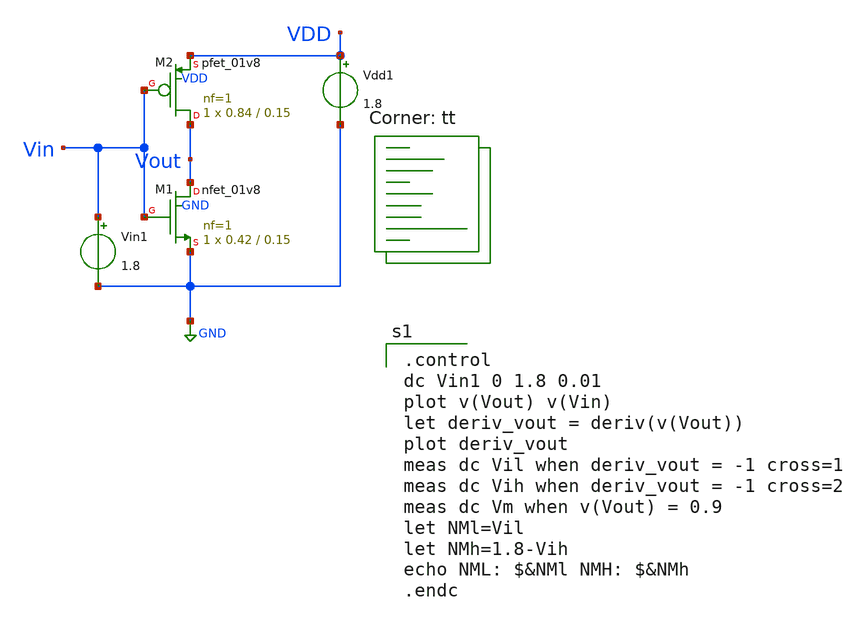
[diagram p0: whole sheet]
** sch_path: tut2/expt2_0/expt2_0.sch
**.subckt expt2_0
XM1 Vout Vin GND GND sky130_fd_pr__nfet_01v8 L=0.15 W=0.42 nf=1 ad='int((nf+1)/2) * W/nf * 0.29' as='int((nf+2)/2) * W/nf * 0.29'
+ pd='2*int((nf+1)/2) * (W/nf + 0.29)' ps='2*int((nf+2)/2) * (W/nf + 0.29)' nrd='0.29 / W' nrs='0.29 / W'
+ sa=0 sb=0 sd=0 mult=1 m=1
Vin1 Vin GND 1.8
XM2 Vout Vin VDD VDD sky130_fd_pr__pfet_01v8 L=0.15 W=0.84 nf=1 ad='int((nf+1)/2) * W/nf * 0.29' as='int((nf+2)/2) * W/nf * 0.29'
+ pd='2*int((nf+1)/2) * (W/nf + 0.29)' ps='2*int((nf+2)/2) * (W/nf + 0.29)' nrd='0.29 / W' nrs='0.29 / W'
+ sa=0 sb=0 sd=0 mult=1 m=1
Vdd1 VDD GND 1.8
**** begin user architecture code
.lib $::SKYWATER_MODELS/sky130.lib.spice tt

.control
dc Vin1 0 1.8 0.01
plot v(Vout) v(Vin)
let deriv_vout = deriv(v(Vout))
plot deriv_vout
meas dc Vil when deriv_vout = -1 cross=1
meas dc Vih when deriv_vout = -1 cross=2
meas dc Vm when v(Vout) = 0.9
let NMl=Vil
let NMh=1.8-Vih
echo NML: $&NMl NMH: $&NMh
.endc

**** end user architecture code
**.ends
.GLOBAL GND
.end
